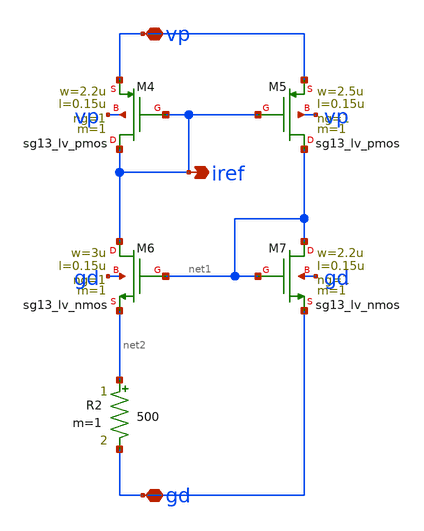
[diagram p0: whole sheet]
** sch_path: charge_pump/curr_source.sch
**.subckt curr_source vp gd iref
*.iopin vp
*.iopin gd
*.opin iref
XM4 iref iref vp vp sg13_lv_pmos w=2.2u l=0.15u ng=1 m=1 mm_ok=1
XM5 net1 iref vp vp sg13_lv_pmos w=2.5u l=0.15u ng=1 m=1 mm_ok=1
XM6 iref net1 net2 gd sg13_lv_nmos w=3u l=0.15u ng=1 m=1 mm_ok=1
XM7 net1 net1 gd gd sg13_lv_nmos w=2.2u l=0.15u ng=1 m=1 mm_ok=1
R2 net2 gd 500 m=1
**.ends
.end
